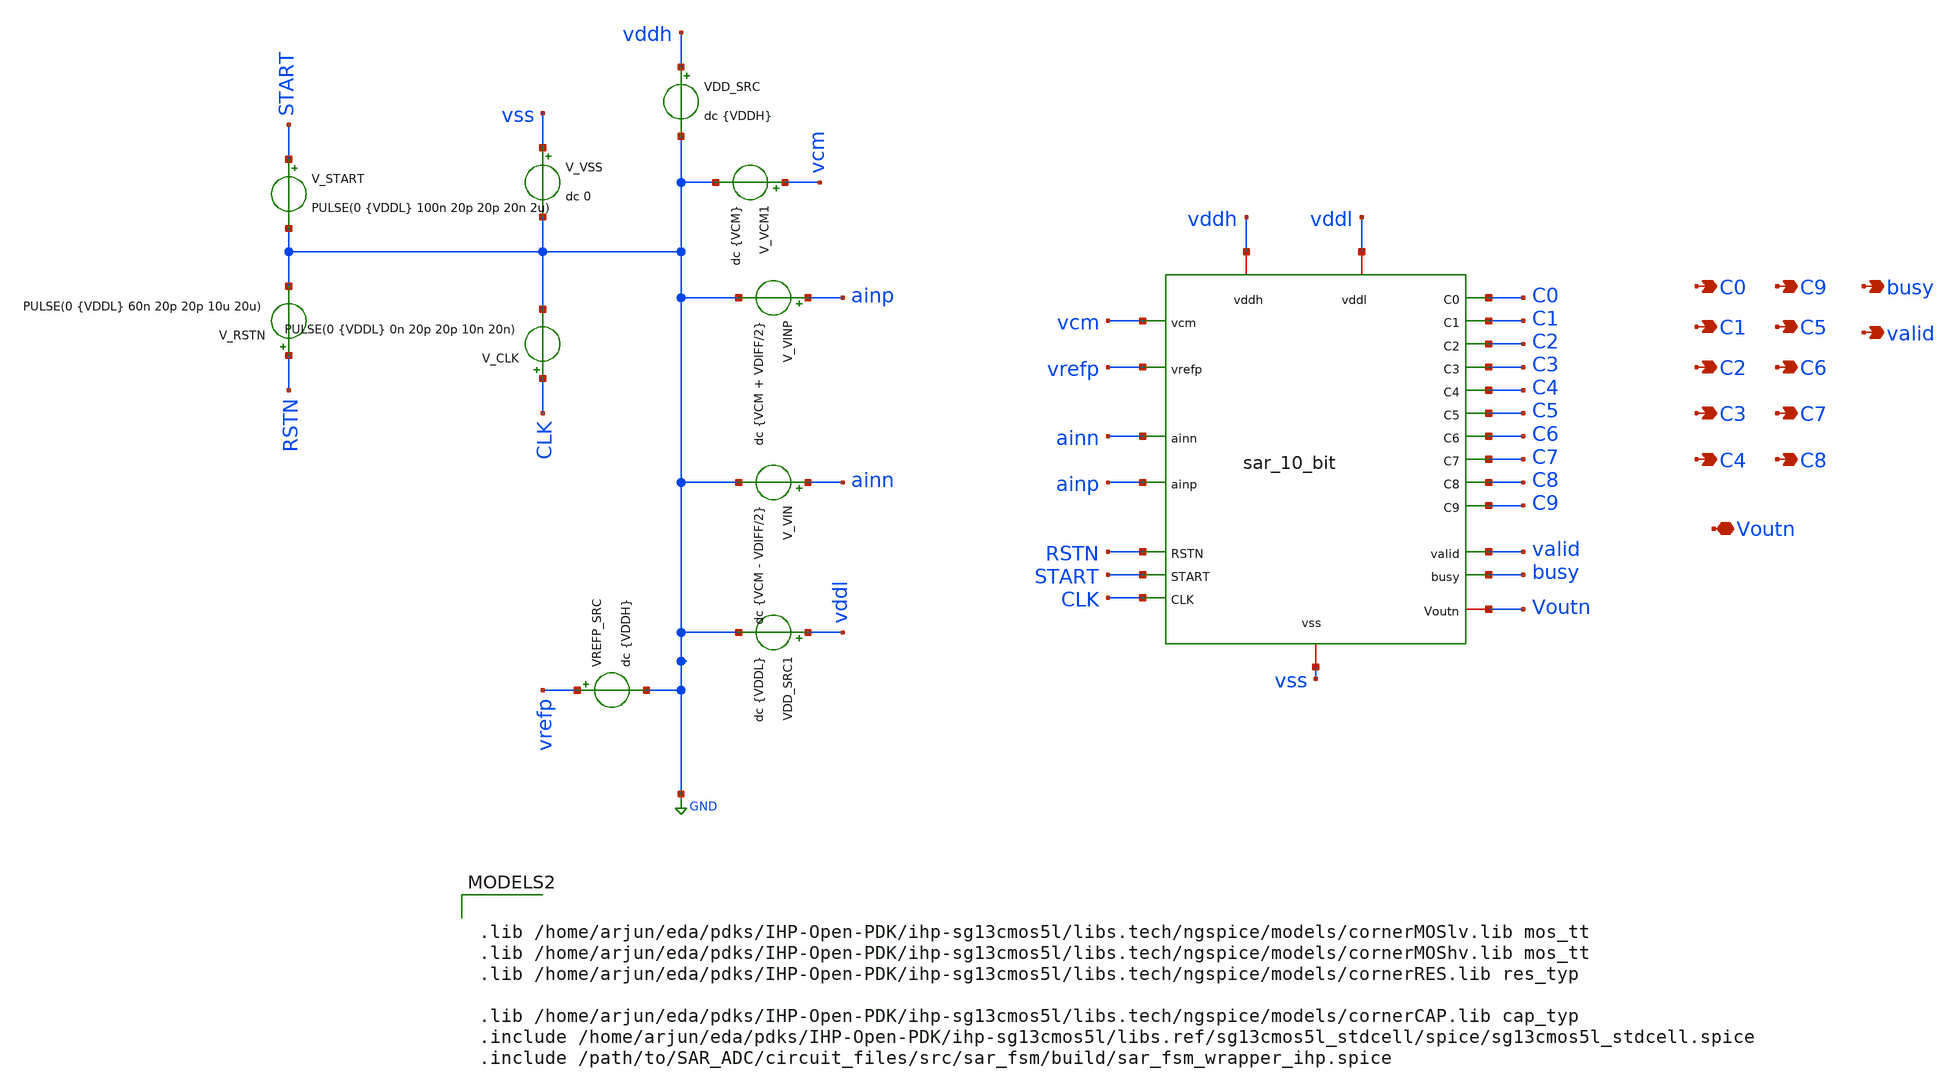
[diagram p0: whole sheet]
** sch_path: circuit_files/sar_adc_test/tb/sar_10_bit_tb.sch
**.subckt sar_10_bit_tb C1 C2 C3 C4 C5 C6 C7 C8 C0 C9 busy valid Voutn
*.opin C1
*.opin C2
*.opin C3
*.opin C4
*.opin C5
*.opin C6
*.opin C7
*.opin C8
*.opin C0
*.opin C9
*.opin busy
*.opin valid
*.iopin Voutn
x1 RSTN busy START valid vcm vrefp ainn ainp CLK C0 C9 C1 C5 C6 C2 C7 C3 C8 C4 vss vddh Voutn vddl
+ sar_10_bit
V_VIN ainn GND dc {VCM - VDIFF/2}
VDD_SRC vddh GND dc {VDDH}
V_VINP ainp GND dc {VCM + VDIFF/2}
V_VSS vss GND dc 0
V_CLK CLK GND PULSE(0 {VDDL} 0n 20p 20p 10n 20n)
V_VCM1 vcm GND dc {VCM}
VREFP_SRC vrefp GND dc {VDDH}
V_RSTN RSTN GND PULSE(0 {VDDL} 60n 20p 20p 10u 20u)
V_START START GND PULSE(0 {VDDL} 100n 20p 20p 20n 2u)
VDD_SRC1 vddl GND dc {VDDL}
**** begin user architecture code

.lib /home/arjun/eda/pdks/IHP-Open-PDK/ihp-sg13cmos5l/libs.tech/ngspice/models/cornerMOSlv.lib mos_tt
.lib /home/arjun/eda/pdks/IHP-Open-PDK/ihp-sg13cmos5l/libs.tech/ngspice/models/cornerMOShv.lib mos_tt
.lib /home/arjun/eda/pdks/IHP-Open-PDK/ihp-sg13cmos5l/libs.tech/ngspice/models/cornerRES.lib res_typ

.lib /home/arjun/eda/pdks/IHP-Open-PDK/ihp-sg13cmos5l/libs.tech/ngspice/models/cornerCAP.lib cap_typ
.include /home/arjun/eda/pdks/IHP-Open-PDK/ihp-sg13cmos5l/libs.ref/sg13cmos5l_stdcell/spice/sg13cmos5l_stdcell.spice
.include /path/to/SAR_ADC/circuit_files/src/sar_fsm/build/sar_fsm_wrapper_ihp.spice




.param VDDH=3.3
.param VDDL=1.2

.param VREF=3.3
.param VCM=1.65

.param NBITS=10
.param Cu=10f

* LSB = 3.3 / 1024 = 3.22265625 mV
.param VDIFF=0


*.options savecurrents
.options reltol=1e-4
.options abstol=1e-12
.options vntol=1e-6

.options method=gear
.options maxord=2

.options plotwinsize=0
.options itl4=500

.save v(valid)

.save v(C9)
.save v(C8)
.save v(C7)
.save v(C6)
.save v(C5)
.save v(C4)
.save v(C3)
.save v(C2)
.save v(C1)
.save v(C0)






.control

set noaskquit
set num_threads=6

setplot const

let npts = 1025

let vin_vec = -1.65 + (3.3/1024)*vector(npts)
let code_vec = 0*vector(npts)
let valid_vec = 0*vector(npts)

let index = 0

echo
echo FULL_10_BIT_SAR_ADC_TRANSFER
echo 1025_INPUT_POINTS


repeat 1025

  let vdiff_now = vin_vec[index]

  let vinp_now = 1.65 + vdiff_now/2
  let vinn_now = 1.65 - vdiff_now/2


  echo
  echo POINT
  print index
  echo VDIFF
  print vdiff_now


  alter V_VINP $&vinp_now
  alter V_VIN  $&vinn_now


  tran 500p 1.30u 0 500p


  meas tran valid_max MAX v(valid) FROM=100n TO=1.30u

  meas tran c9v FIND v(C9) AT=1.28u
  meas tran c8v FIND v(C8) AT=1.28u
  meas tran c7v FIND v(C7) AT=1.28u
  meas tran c6v FIND v(C6) AT=1.28u
  meas tran c5v FIND v(C5) AT=1.28u
  meas tran c4v FIND v(C4) AT=1.28u
  meas tran c3v FIND v(C3) AT=1.28u
  meas tran c2v FIND v(C2) AT=1.28u
  meas tran c1v FIND v(C1) AT=1.28u
  meas tran c0v FIND v(C0) AT=1.28u


  let adc_code = 512*(c9v gt 0.6) + 256*(c8v gt 0.6) + 128*(c7v gt 0.6) + 64*(c6v gt 0.6) + 32*(c5v
+ gt 0.6) + 16*(c4v gt 0.6) + 8*(c3v gt 0.6) + 4*(c2v gt 0.6) + 2*(c1v gt 0.6) + (c0v gt 0.6)

  let valid_ok = valid_max gt 0.6


  let code_vec[index] = adc_code
  let valid_vec[index] = valid_ok


  echo CODE
  print adc_code

  echo VALID
  print valid_ok


  destroy $curplot

  setplot const

  let index = index + 1

end


setplot const


echo
echo FULL_TRANSFER_COMPLETE

setscale code_vec vin_vec
setscale valid_vec vin_vec

set wr_singlescale
set wr_vecnames

option numdgt=10

wrdata adc_full_transfer.dat code_vec valid_vec


plot code_vec vs vin_vec linplot xlimit -1.65 1.65 ylimit 0 1023 xlabel VDIFF_V ylabel ADC_CODE
+ title FULL_10_BIT_SAR_ADC_TRANSFER


echo
echo Results_written_to_adc_full_transfer.dat
echo

rusage

.endc


**** end user architecture code
**.ends
.GLOBAL GND
.end
